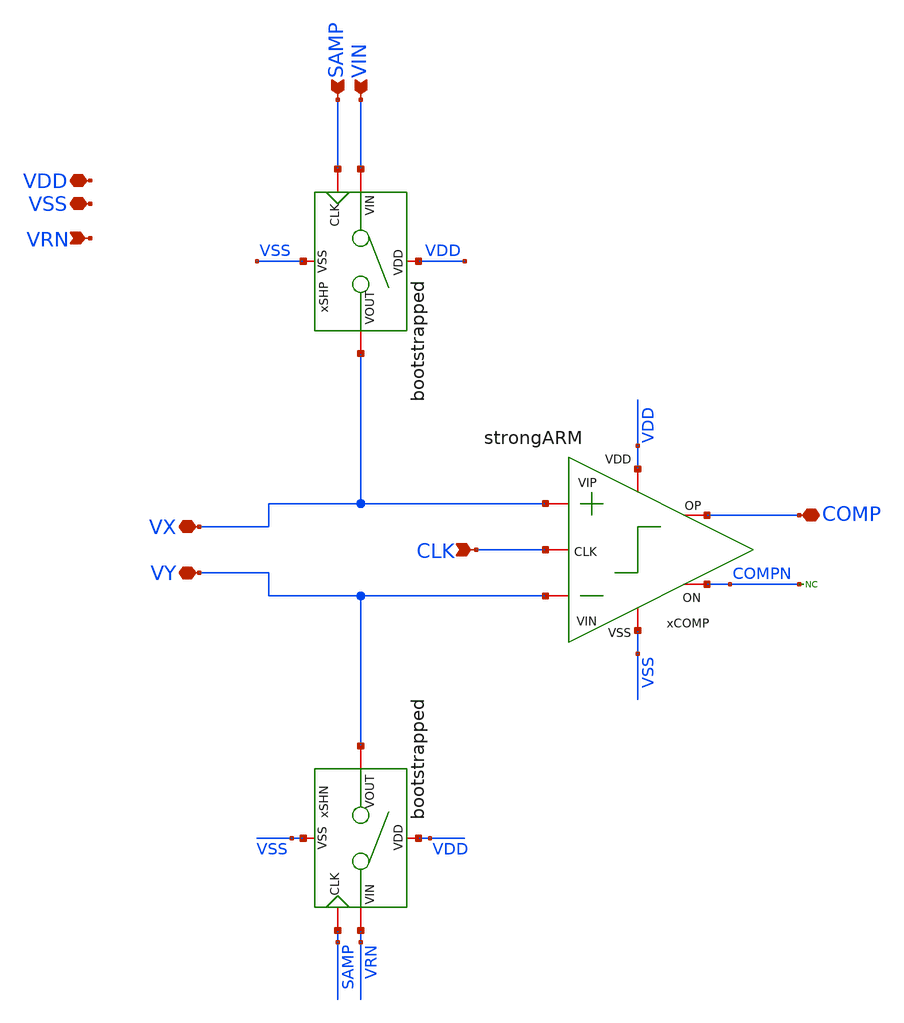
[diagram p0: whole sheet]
** sch_path: designs/sar_adc/top/comp_and_samp/xschem/comp_and_samp.sch
**.subckt comp_and_samp VIN VY VX SAMP COMP CLK VSS VDD VRN
*.ipin VIN
*.iopin VY
*.iopin VX
*.ipin SAMP
*.iopin COMP
*.ipin CLK
*.iopin VSS
*.iopin VDD
*.ipin VRN
xSHP VDD VSS SAMP VIN VX bootstrapped
xSHN VDD VSS SAMP VRN VY bootstrapped
xCOMP VDD CLK COMPN COMP VY VX VSS strongARM
* noconn COMPN
**.ends
.end
